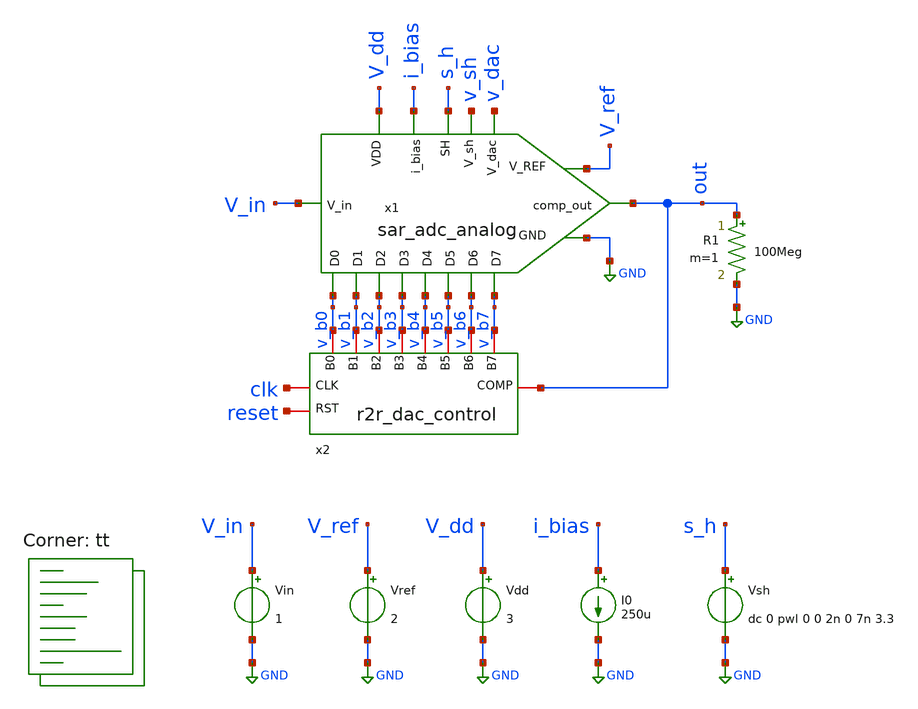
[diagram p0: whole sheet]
** sch_path: xschem/tb_sar_adc_perf.sch
**.subckt tb_sar_adc_perf
Vin V_in GND 1
x1 s_h V_in out i_bias v_b0 V_dd v_b1 v_b2 v_b3 GND v_b4 V_ref v_b5 v_b6 v_b7 v_sh v_dac
+ sar_adc_analog
Vref V_ref GND 2
R1 out GND 100Meg m=1
Vdd V_dd GND 3
I0 i_bias GND 250u
x2 reset clk out v_b7 v_b6 v_b5 v_b4 v_b3 v_b2 v_b1 v_b0 r2r_dac_control
Vsh s_h GND dc 0 pwl 0 0 2n 0 7n 3.3
**** begin user architecture code
.lib $::SKYWATER_MODELS/sky130.lib.spice tt


.option chgtol=4e-16

*.param TEMPGAUSS = agauss(30, 40, 1)
*.option temp = 'TEMPGAUSS'
*.param DELTA = 0.002

* .param vdda 3.3
.option TNOM=27 GMIN=1e-15 reltol=1e-3 method=gear
.param TRF = 100p
.param AVDD = 3.3
.param PERIOD_CLK = 40n
.param PW_CLK = PERIOD_CLK/2



* VCLK clk 0 dc 0 pulse (0 3.3 0 10p 10p 500n 1u)
VCLK clk 0 dc 0 pulse (0 {AVDD} 0 {TRF} {TRF} {PW_CLK} {PERIOD_CLK})
VRESET reset 0 dc {AVDD} pwl 0 {AVDD} {PW_CLK*4} {AVDD} {PW_CLK*2 + 1n} 0


.control

set num_threads=8
unset askquit



*- Override the default digital output bridge.
pre_set auto_bridge_d_out =
     + ( ".model auto_dac dac_bridge(out_low = 0.0 out_high = 1.8)"
     +   "auto_bridge%d [ %s ] [ %s ] auto_dac" )


let vvin = 2    ; input voltage
let index = 0                     ; loop index in plot 'const'
let loops = 256                     ; number of loops, vector in plot 'const'
let lsb = 0.0078125
repeat $&loops                    ; loop start
  save all
  alter Vin $&vvin                ; alter the voltage Vcc
  tran 1n 450n
  write tb_sar_adc_perf.raw
  set appendwrite
  let vvin = vvin - lsb
  let index = index + 1
  reset
end

.endc




*.include ./../cosim/r2r_dac_control.spice

.subckt r2r_dac_control reset clk comp b7 b6 b5 b4 b3 b2 b1 b0

adut [clk  reset  comp  ]  [b7  b6  b5  b4  b3  b2  b1  b0  ] null r2r_ctrl

.model r2r_ctrl d_cosim
+ simulation="/home/ttuser/tinytapeout/TT_Project/verilog/sim/r2r_dac_control.so" delay=10p
.ends r2r_dac_control


**** end user architecture code
**.ends
.GLOBAL GND
.end
